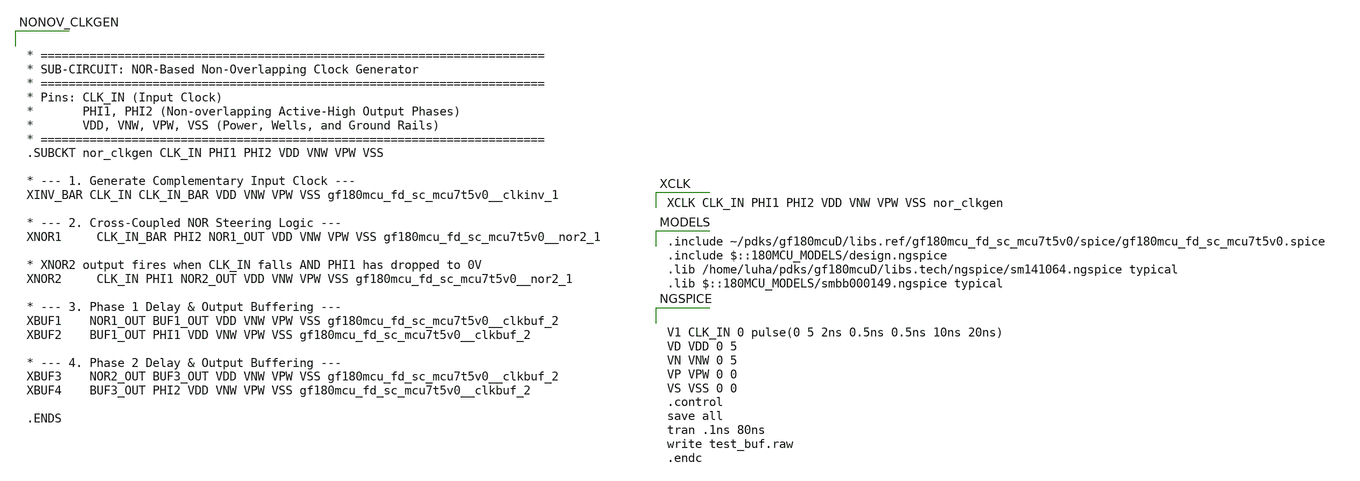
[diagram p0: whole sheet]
** sch_path: GF180_cells/NonOvCLKGen/design/NonOvCLKGen_TB.sch
**.subckt NonOvCLKGen_TB
**** begin user architecture code
 .include ~/pdks/gf180mcuD/libs.ref/gf180mcu_fd_sc_mcu7t5v0/spice/gf180mcu_fd_sc_mcu7t5v0.spice
.include $::180MCU_MODELS/design.ngspice
.lib /home/luha/pdks/gf180mcuD/libs.tech/ngspice/sm141064.ngspice typical
.lib $::180MCU_MODELS/smbb000149.ngspice typical

XCLK CLK_IN PHI1 PHI2 VDD VNW VPW VSS nor_clkgen



V1 CLK_IN 0 pulse(0 5 2ns 0.5ns 0.5ns 10ns 20ns)
VD VDD 0 5
VN VNW 0 5
VP VPW 0 0
VS VSS 0 0
.control
save all
tran .1ns 80ns
write test_buf.raw
.endc




* ========================================================================
* SUB-CIRCUIT: NOR-Based Non-Overlapping Clock Generator
* ========================================================================
* Pins: CLK_IN (Input Clock)
*       PHI1, PHI2 (Non-overlapping Active-High Output Phases)
*       VDD, VNW, VPW, VSS (Power, Wells, and Ground Rails)
* ========================================================================
.SUBCKT nor_clkgen CLK_IN PHI1 PHI2 VDD VNW VPW VSS

* --- 1. Generate Complementary Input Clock ---
XINV_BAR CLK_IN CLK_IN_BAR VDD VNW VPW VSS gf180mcu_fd_sc_mcu7t5v0__clkinv_1

* --- 2. Cross-Coupled NOR Steering Logic ---
XNOR1	 CLK_IN_BAR PHI2 NOR1_OUT VDD VNW VPW VSS gf180mcu_fd_sc_mcu7t5v0__nor2_1

* XNOR2 output fires when CLK_IN falls AND PHI1 has dropped to 0V
XNOR2	 CLK_IN PHI1 NOR2_OUT VDD VNW VPW VSS gf180mcu_fd_sc_mcu7t5v0__nor2_1

* --- 3. Phase 1 Delay & Output Buffering ---
XBUF1    NOR1_OUT BUF1_OUT VDD VNW VPW VSS gf180mcu_fd_sc_mcu7t5v0__clkbuf_2
XBUF2    BUF1_OUT PHI1 VDD VNW VPW VSS gf180mcu_fd_sc_mcu7t5v0__clkbuf_2

* --- 4. Phase 2 Delay & Output Buffering ---
XBUF3    NOR2_OUT BUF3_OUT VDD VNW VPW VSS gf180mcu_fd_sc_mcu7t5v0__clkbuf_2
XBUF4    BUF3_OUT PHI2 VDD VNW VPW VSS gf180mcu_fd_sc_mcu7t5v0__clkbuf_2

.ENDS


**** end user architecture code
**.ends
.end
